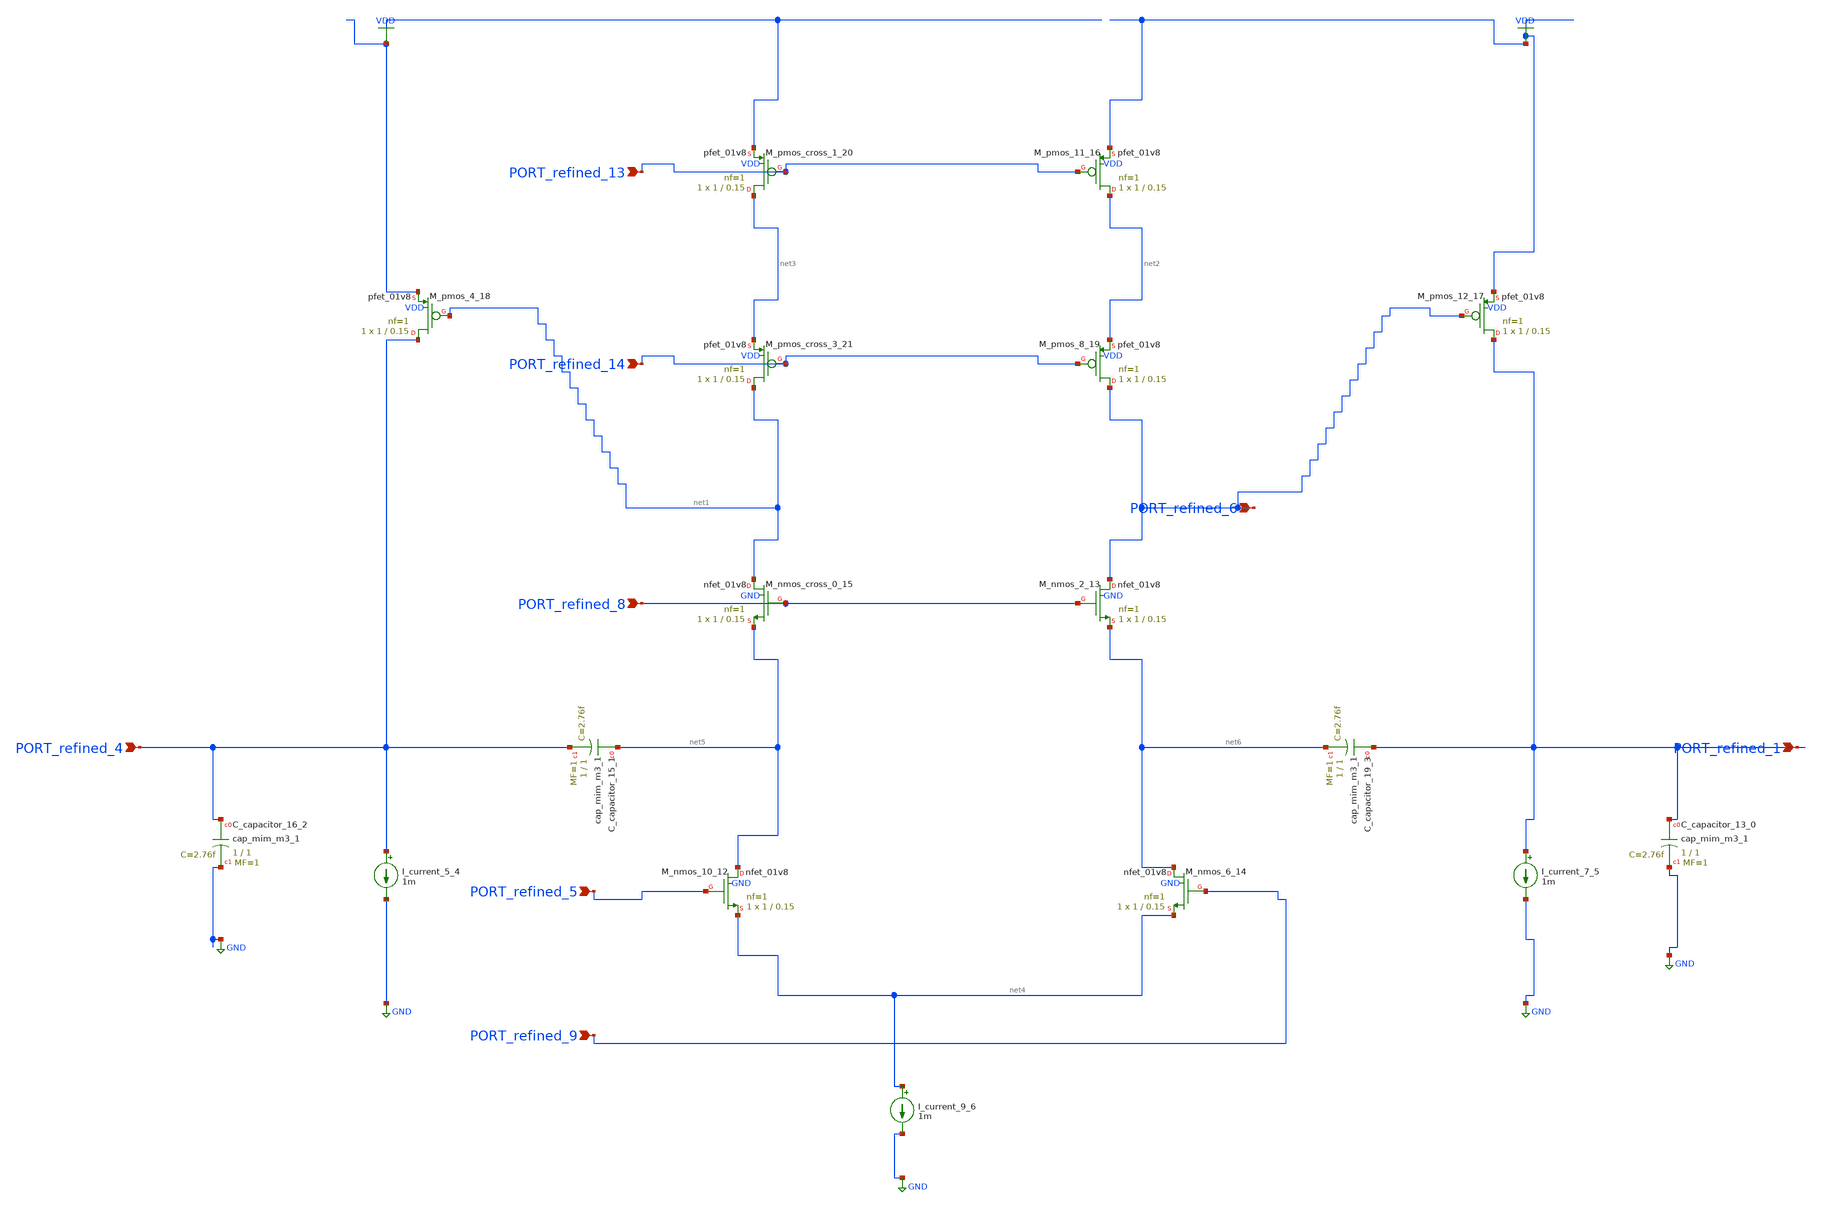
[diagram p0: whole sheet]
** sch_path: schematics/AMSNet/738.sch
**.subckt 738 PORT_refined_5 PORT_refined_1 PORT_refined_4 PORT_refined_9 PORT_refined_8
*+ PORT_refined_14 PORT_refined_6 PORT_refined_13
*.ipin PORT_refined_5
*.ipin PORT_refined_1
*.ipin PORT_refined_4
*.ipin PORT_refined_9
*.ipin PORT_refined_8
*.ipin PORT_refined_14
*.ipin PORT_refined_6
*.ipin PORT_refined_13
XC_capacitor_13_0 PORT_refined_1 GND sky130_fd_pr__cap_mim_m3_1 W=1 L=1 MF=1 m=1
XC_capacitor_15_1 net5 PORT_refined_4 sky130_fd_pr__cap_mim_m3_1 W=1 L=1 MF=1 m=1
XC_capacitor_16_2 PORT_refined_4 GND sky130_fd_pr__cap_mim_m3_1 W=1 L=1 MF=1 m=1
XC_capacitor_19_3 PORT_refined_1 net6 sky130_fd_pr__cap_mim_m3_1 W=1 L=1 MF=1 m=1
I_current_5_4 PORT_refined_4 GND 1m
I_current_7_5 PORT_refined_1 GND 1m
I_current_9_6 net4 GND 1m
XM_nmos_10_12 net5 PORT_refined_5 net4 GND sky130_fd_pr__nfet_01v8 L=0.15 W=1 nf=1 ad='int((1 + 1)/2) * 1 / 1 * 0.29'
+ as='int((1 + 2)/2) * 1 / 1 * 0.29' pd='2*int((1 + 1)/2) * (1 / 1 + 0.29)' ps='2*int((1 + 2)/2) * (1 / 1 + 0.29)'
+ nrd='0.29 / 1 ' nrs='0.29 / 1 ' sa=0 sb=0 sd=0 mult=1 m=1
XM_nmos_2_13 PORT_refined_6 PORT_refined_8 net6 GND sky130_fd_pr__nfet_01v8 L=0.15 W=1 nf=1 ad='int((1 + 1)/2) * 1 / 1 * 0.29'
+ as='int((1 + 2)/2) * 1 / 1 * 0.29' pd='2*int((1 + 1)/2) * (1 / 1 + 0.29)' ps='2*int((1 + 2)/2) * (1 / 1 + 0.29)'
+ nrd='0.29 / 1 ' nrs='0.29 / 1 ' sa=0 sb=0 sd=0 mult=1 m=1
XM_nmos_6_14 net6 PORT_refined_9 net4 GND sky130_fd_pr__nfet_01v8 L=0.15 W=1 nf=1 ad='int((1 + 1)/2) * 1 / 1 * 0.29'
+ as='int((1 + 2)/2) * 1 / 1 * 0.29' pd='2*int((1 + 1)/2) * (1 / 1 + 0.29)' ps='2*int((1 + 2)/2) * (1 / 1 + 0.29)'
+ nrd='0.29 / 1 ' nrs='0.29 / 1 ' sa=0 sb=0 sd=0 mult=1 m=1
XM_nmos_cross_0_15 net1 PORT_refined_8 net5 GND sky130_fd_pr__nfet_01v8 L=0.15 W=1 nf=1 ad='int((1 + 1)/2) * 1 / 1 * 0.29'
+ as='int((1 + 2)/2) * 1 / 1 * 0.29' pd='2*int((1 + 1)/2) * (1 / 1 + 0.29)' ps='2*int((1 + 2)/2) * (1 / 1 + 0.29)'
+ nrd='0.29 / 1 ' nrs='0.29 / 1 ' sa=0 sb=0 sd=0 mult=1 m=1
XM_pmos_11_16 net2 PORT_refined_13 VDD VDD sky130_fd_pr__pfet_01v8 L=0.15 W=1 nf=1 ad='int((1 + 1)/2) * 1 / 1 * 0.29'
+ as='int((1 + 2)/2) * 1 / 1 * 0.29' pd='2*int((1 + 1)/2) * (1 / 1 + 0.29)' ps='2*int((1 + 2)/2) * (1 / 1 + 0.29)'
+ nrd='0.29 / 1 ' nrs='0.29 / 1 ' sa=0 sb=0 sd=0 mult=1 m=1
XM_pmos_12_17 PORT_refined_1 PORT_refined_6 VDD VDD sky130_fd_pr__pfet_01v8 L=0.15 W=1 nf=1 ad='int((1 + 1)/2) * 1 / 1 * 0.29'
+ as='int((1 + 2)/2) * 1 / 1 * 0.29' pd='2*int((1 + 1)/2) * (1 / 1 + 0.29)' ps='2*int((1 + 2)/2) * (1 / 1 + 0.29)'
+ nrd='0.29 / 1 ' nrs='0.29 / 1 ' sa=0 sb=0 sd=0 mult=1 m=1
XM_pmos_4_18 PORT_refined_4 net1 VDD VDD sky130_fd_pr__pfet_01v8 L=0.15 W=1 nf=1 ad='int((1 + 1)/2) * 1 / 1 * 0.29'
+ as='int((1 + 2)/2) * 1 / 1 * 0.29' pd='2*int((1 + 1)/2) * (1 / 1 + 0.29)' ps='2*int((1 + 2)/2) * (1 / 1 + 0.29)'
+ nrd='0.29 / 1 ' nrs='0.29 / 1 ' sa=0 sb=0 sd=0 mult=1 m=1
XM_pmos_8_19 PORT_refined_6 PORT_refined_14 net2 VDD sky130_fd_pr__pfet_01v8 L=0.15 W=1 nf=1 ad='int((1 + 1)/2) * 1 / 1 * 0.29'
+ as='int((1 + 2)/2) * 1 / 1 * 0.29' pd='2*int((1 + 1)/2) * (1 / 1 + 0.29)' ps='2*int((1 + 2)/2) * (1 / 1 + 0.29)'
+ nrd='0.29 / 1 ' nrs='0.29 / 1 ' sa=0 sb=0 sd=0 mult=1 m=1
XM_pmos_cross_1_20 net3 PORT_refined_13 VDD VDD sky130_fd_pr__pfet_01v8 L=0.15 W=1 nf=1 ad='int((1 + 1)/2) * 1 / 1 * 0.29'
+ as='int((1 + 2)/2) * 1 / 1 * 0.29' pd='2*int((1 + 1)/2) * (1 / 1 + 0.29)' ps='2*int((1 + 2)/2) * (1 / 1 + 0.29)'
+ nrd='0.29 / 1 ' nrs='0.29 / 1 ' sa=0 sb=0 sd=0 mult=1 m=1
XM_pmos_cross_3_21 net1 PORT_refined_14 net3 VDD sky130_fd_pr__pfet_01v8 L=0.15 W=1 nf=1 ad='int((1 + 1)/2) * 1 / 1 * 0.29'
+ as='int((1 + 2)/2) * 1 / 1 * 0.29' pd='2*int((1 + 1)/2) * (1 / 1 + 0.29)' ps='2*int((1 + 2)/2) * (1 / 1 + 0.29)'
+ nrd='0.29 / 1 ' nrs='0.29 / 1 ' sa=0 sb=0 sd=0 mult=1 m=1
**.ends
.GLOBAL GND
.GLOBAL VDD
.end
